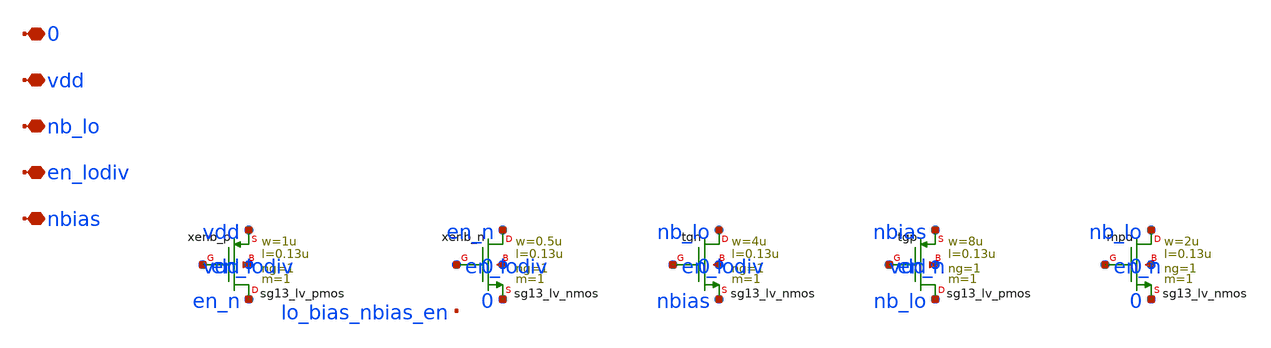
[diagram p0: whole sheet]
** sch_path: analog/lo/sch/lo_bias.sch
**.subckt lo_bias nbias en_lodiv nb_lo vdd 0
*.iopin nbias
*.iopin en_lodiv
*.iopin nb_lo
*.iopin vdd
*.iopin 0
Xxenb_p en_n en_lodiv vdd vdd sg13_lv_pmos w=1u l=0.13u ng=1 m=1 mm_ok=1
Xxenb_n en_n en_lodiv 0 0 sg13_lv_nmos w=0.5u l=0.13u ng=1 m=1 mm_ok=1
Xtgn nb_lo en_lodiv nbias 0 sg13_lv_nmos w=4u l=0.13u ng=1 m=1 mm_ok=1
Xtgp nb_lo en_n nbias vdd sg13_lv_pmos w=8u l=0.13u ng=1 m=1 mm_ok=1
Xmpd nb_lo en_n 0 0 sg13_lv_nmos w=2u l=0.13u ng=1 m=1 mm_ok=1
**.ends
.end
